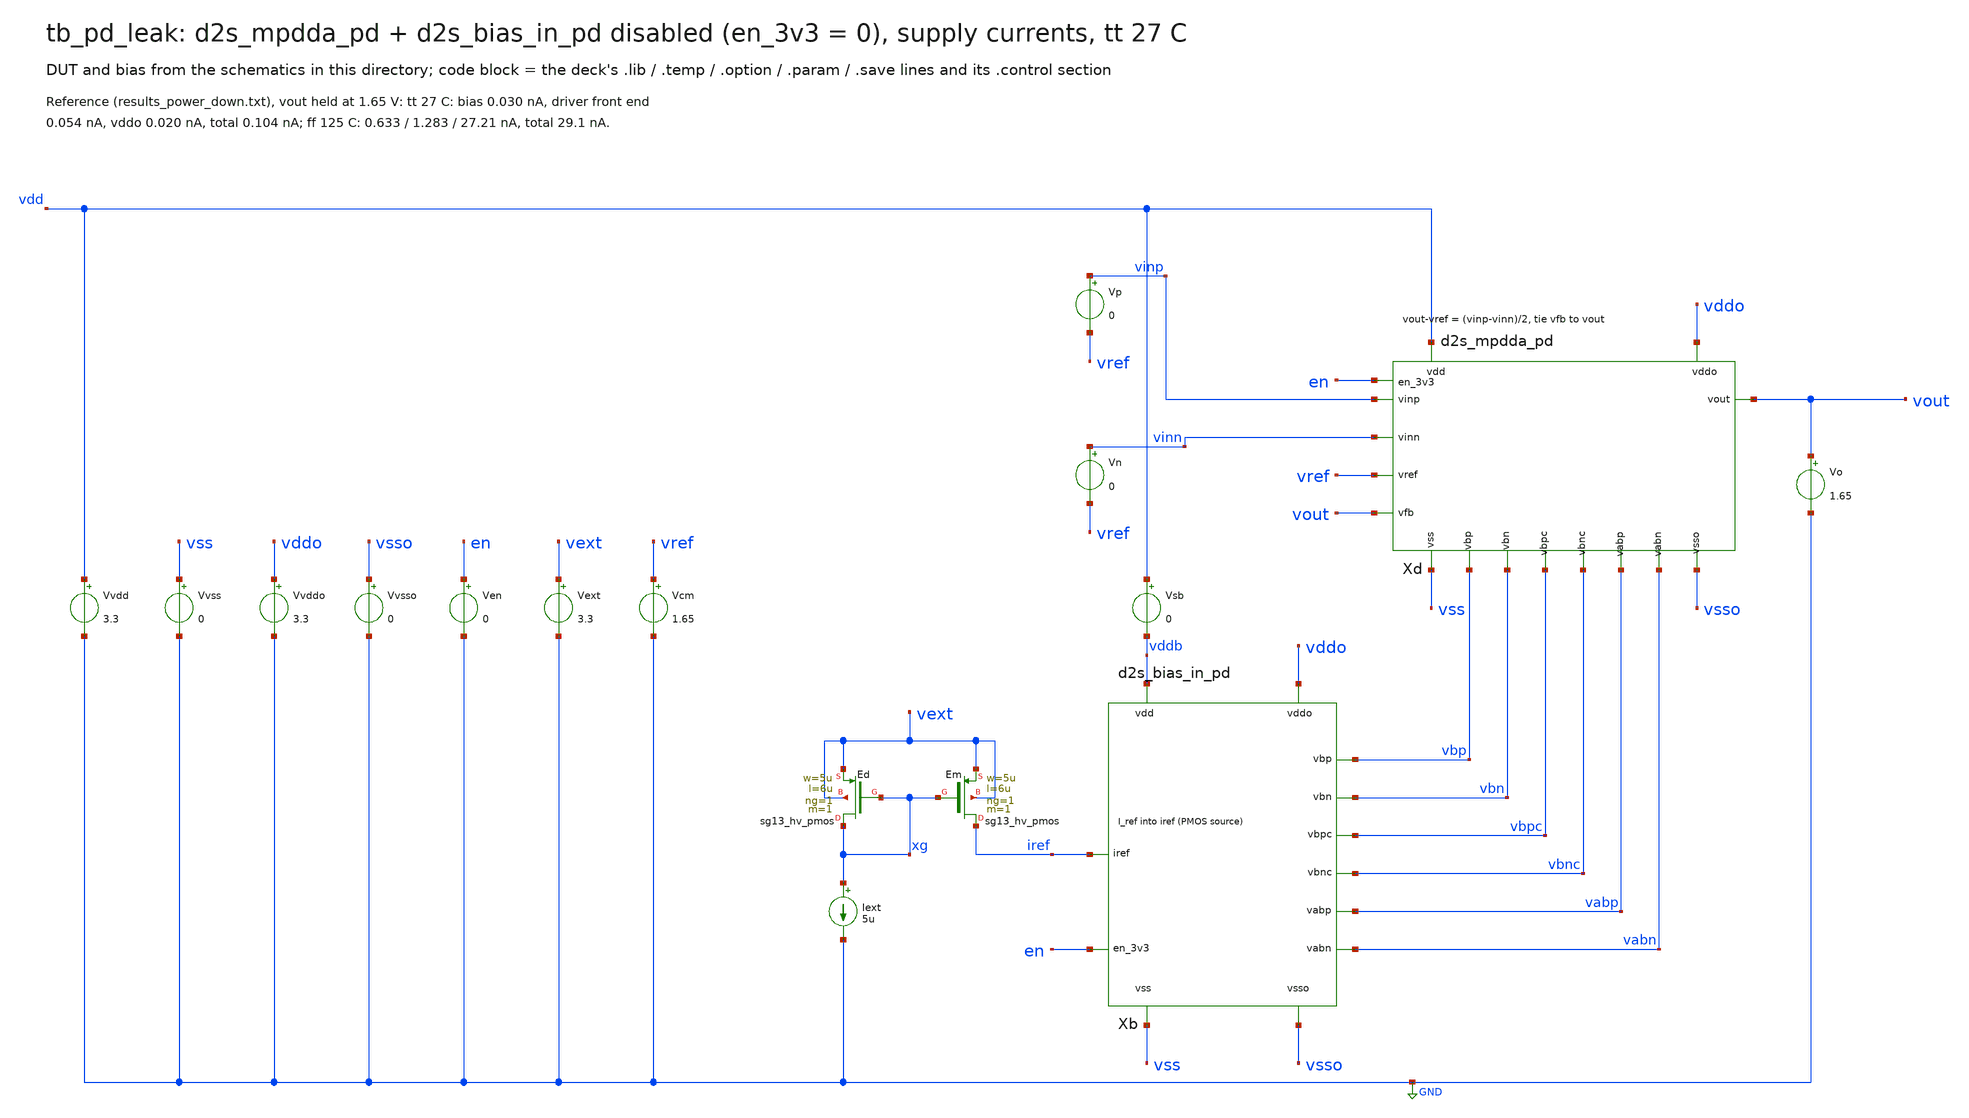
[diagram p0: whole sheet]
** sch_path: sudelbuecher/design_considerations/class_ab_pad_driver/power_down/xschem/tb_pd_leak.sch
**.subckt tb_pd_leak
Vvdd vdd GND 3.3
Vvss vss GND 0
Vvddo vddo GND 3.3
Vvsso vsso GND 0
Ven en GND 0
Vext vext GND 3.3
Vcm vref GND 1.65
Xb vddb vss vddo vsso iref vbp vbn vbpc vbnc vabp vabn en d2s_bias_in_pd
Xd vdd vss vddo vsso vinp vinn vref vout vout vbp vbn vbpc vbnc vabp vabn en d2s_mpdda_pd
Vsb vdd vddb 0
Vp vinp vref 0
Vn vinn vref 0
XEd xg xg vext vext sg13_hv_pmos w=5u l=6u ng=1 m=1 mm_ok=1
XEm iref xg vext vext sg13_hv_pmos w=5u l=6u ng=1 m=1 mm_ok=1
Iext xg GND 5u
Vo vout GND 1.65
**** begin user architecture code

.lib cornerMOShv.lib mos_tt
.lib cornerRES.lib res_typ
.lib cornerCAP.lib cap_typ
.temp 27
.control
op
let ibias = i(vsb)
let idrv = -i(vvdd) - i(vsb)
let iddo = -i(vvddo)
let itot = -i(vvdd) - i(vvddo)
let vsg_op = v(vddo) - v(xd.a)
let vgs_on = v(xd.b) - v(vsso)
print ibias idrv iddo itot vsg_op vgs_on
print v(vbp) v(vbpc) v(vabp) v(vabn) v(vbn) v(vbnc)
.endc

**** end user architecture code
**.ends
.GLOBAL GND
.end
